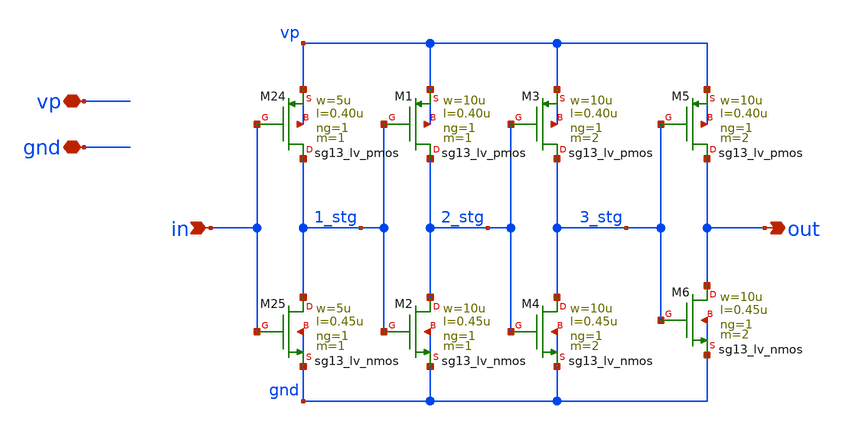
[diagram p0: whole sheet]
** sch_path: schematics/vco/vco_cell/0_buf.sch
**.subckt 0_buf in out vp gnd
*.ipin in
*.opin out
*.iopin vp
*.iopin gnd
XM24 1_stg in vp vp sg13_lv_pmos w=5u l=0.40u ng=1 m=1 mm_ok=1
XM25 1_stg in gnd gnd sg13_lv_nmos w=5u l=0.45u ng=1 m=1 mm_ok=1
XM1 2_stg 1_stg vp vp sg13_lv_pmos w=10u l=0.40u ng=1 m=1 mm_ok=1
XM2 2_stg 1_stg gnd gnd sg13_lv_nmos w=10u l=0.45u ng=1 m=1 mm_ok=1
XM3 3_stg 2_stg vp vp sg13_lv_pmos w=10u l=0.40u ng=1 m=2 mm_ok=1
XM4 3_stg 2_stg gnd gnd sg13_lv_nmos w=10u l=0.45u ng=1 m=2 mm_ok=1
XM5 out 3_stg vp vp sg13_lv_pmos w=10u l=0.40u ng=1 m=2 mm_ok=1
XM6 out 3_stg gnd gnd sg13_lv_nmos w=10u l=0.45u ng=1 m=2 mm_ok=1
**.ends
.end
